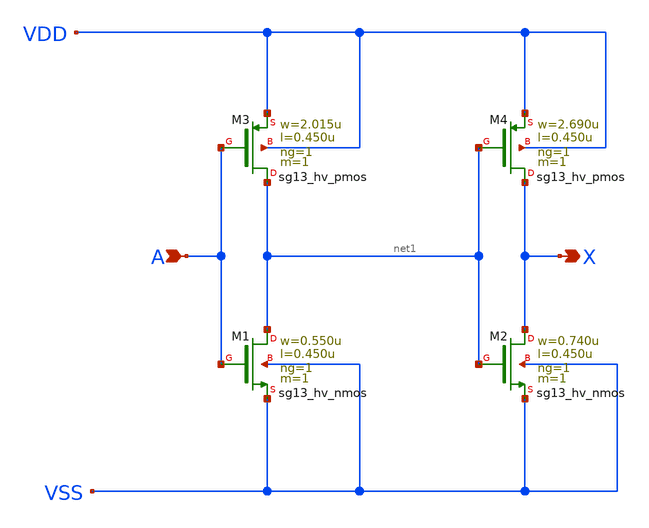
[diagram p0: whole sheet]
** sch_path: ihp-sg13g2/libs.ref/sg13g2_stdcell_hv/sch/xschem/sg13g2_hv_buf_1.sch
* Copyright 2023 IHP PDK Authors
* Licensed under the Apache License, Version 2.0 (the "License");
* you may not use this file except in compliance with the License.
* You may obtain a copy of the License at
* https://www.apache.org/licenses/LICENSE-2.0
* Unless required by applicable law or agreed to in writing, software
* distributed under the License is distributed on an "AS IS" BASIS,
* WITHOUT WARRANTIES OR CONDITIONS OF ANY KIND, either express or implied.
* See the License for the specific language governing permissions and
* limitations under the License.
**.subckt sg13g2_hv_buf_1 A X
*.ipin A
*.opin X
XM1 net1 A VSS VSS sg13_hv_nmos w=0.550u l=0.450u ng=1 m=1 mm_ok=1
XM2 X net1 VSS VSS sg13_hv_nmos w=0.740u l=0.450u ng=1 m=1 mm_ok=1
XM3 net1 A VDD VDD sg13_hv_pmos w=2.015u l=0.450u ng=1 m=1 mm_ok=1
XM4 X net1 VDD VDD sg13_hv_pmos w=2.690u l=0.450u ng=1 m=1 mm_ok=1
**.ends
.end
